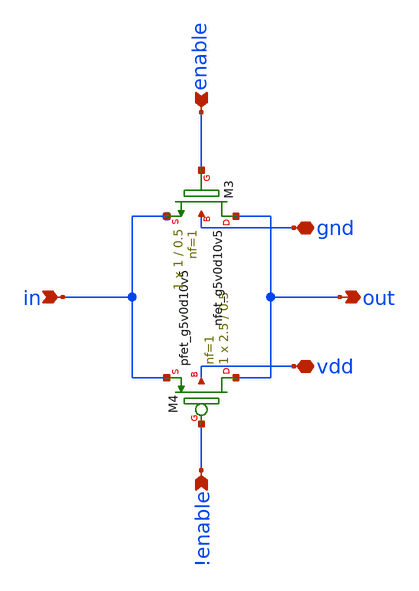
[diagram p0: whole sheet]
** sch_path: sky130_cells/RDAC/Design/sky130_Vinj_TGATE.sch
**.subckt sky130_Vinj_TGATE in out enable vdd gnd !enable
*.ipin in
*.opin out
*.ipin enable
*.iopin vdd
*.iopin gnd
*.ipin !enable
XM4 out !enable in vdd sky130_fd_pr__pfet_g5v0d10v5 L=0.5 W=2.5 nf=1 ad='int((nf+1)/2) * W/nf * 0.29'
+ as='int((nf+2)/2) * W/nf * 0.29' pd='2*int((nf+1)/2) * (W/nf + 0.29)' ps='2*int((nf+2)/2) * (W/nf + 0.29)'
+ nrd='0.29 / W' nrs='0.29 / W' sa=0 sb=0 sd=0 mult=1 m=1
XM3 out enable in gnd sky130_fd_pr__nfet_g5v0d10v5 L=0.5 W=1 nf=1 ad='int((nf+1)/2) * W/nf * 0.29' as='int((nf+2)/2) * W/nf * 0.29'
+ pd='2*int((nf+1)/2) * (W/nf + 0.29)' ps='2*int((nf+2)/2) * (W/nf + 0.29)' nrd='0.29 / W' nrs='0.29 / W'
+ sa=0 sb=0 sd=0 mult=1 m=1
**.ends
.end
